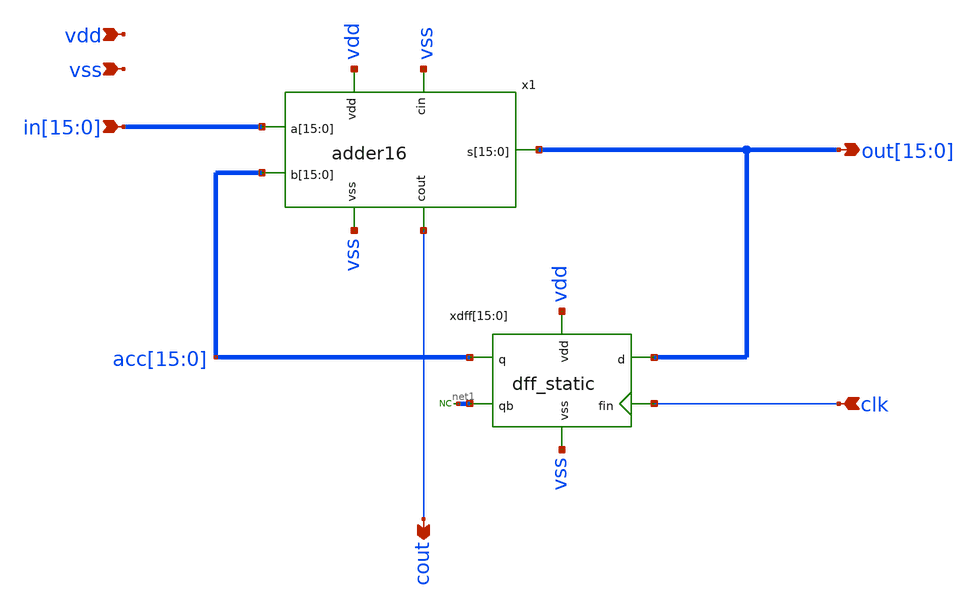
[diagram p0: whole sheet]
** sch_path: xschem/integrator16.sch
**.subckt integrator16
*+ in[15],in[14],in[13],in[12],in[11],in[10],in[9],in[8],in[7],in[6],in[5],in[4],in[3],in[2],in[1],in[0]
*+ out[15],out[14],out[13],out[12],out[11],out[10],out[9],out[8],out[7],out[6],out[5],out[4],out[3],out[2],out[1],out[0] clk cout vdd vss
*.ipin
*+ in[15],in[14],in[13],in[12],in[11],in[10],in[9],in[8],in[7],in[6],in[5],in[4],in[3],in[2],in[1],in[0]
*.opin
*+ out[15],out[14],out[13],out[12],out[11],out[10],out[9],out[8],out[7],out[6],out[5],out[4],out[3],out[2],out[1],out[0]
*.ipin clk
*.opin cout
*.ipin vdd
*.ipin vss
x1 vss vdd vss in[15] in[14] in[13] in[12] in[11] in[10] in[9] in[8] in[7] in[6] in[5] in[4] in[3]
+ in[2] in[1] in[0] acc[15] acc[14] acc[13] acc[12] acc[11] acc[10] acc[9] acc[8] acc[7] acc[6] acc[5]
+ acc[4] acc[3] acc[2] acc[1] acc[0] out[15] out[14] out[13] out[12] out[11] out[10] out[9] out[8] out[7]
+ out[6] out[5] out[4] out[3] out[2] out[1] out[0] cout adder16
xdff[15] vdd net1[15] acc[15] clk out[15] vss dff_static
xdff[14] vdd net1[14] acc[14] clk out[14] vss dff_static
xdff[13] vdd net1[13] acc[13] clk out[13] vss dff_static
xdff[12] vdd net1[12] acc[12] clk out[12] vss dff_static
xdff[11] vdd net1[11] acc[11] clk out[11] vss dff_static
xdff[10] vdd net1[10] acc[10] clk out[10] vss dff_static
xdff[9] vdd net1[9] acc[9] clk out[9] vss dff_static
xdff[8] vdd net1[8] acc[8] clk out[8] vss dff_static
xdff[7] vdd net1[7] acc[7] clk out[7] vss dff_static
xdff[6] vdd net1[6] acc[6] clk out[6] vss dff_static
xdff[5] vdd net1[5] acc[5] clk out[5] vss dff_static
xdff[4] vdd net1[4] acc[4] clk out[4] vss dff_static
xdff[3] vdd net1[3] acc[3] clk out[3] vss dff_static
xdff[2] vdd net1[2] acc[2] clk out[2] vss dff_static
xdff[1] vdd net1[1] acc[1] clk out[1] vss dff_static
xdff[0] vdd net1[0] acc[0] clk out[0] vss dff_static
* noconn #net1
**.ends
.end
